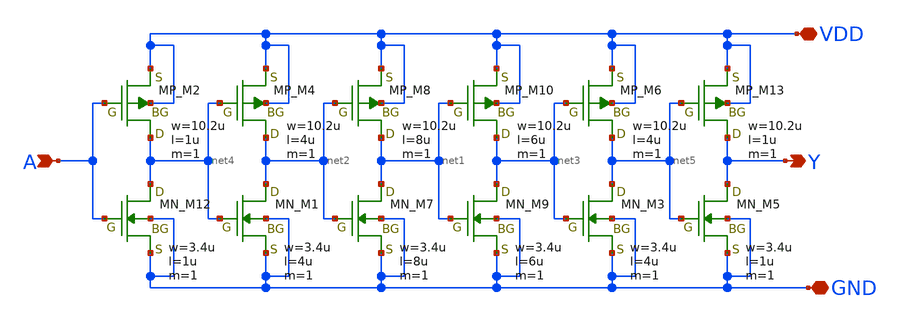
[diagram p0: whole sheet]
** sch_path: libs.tech/xschem/TR-1um_5_stdcell/DEL2.sch
**.subckt DEL2 A Y VDD GND
*.ipin A
*.opin Y
*.iopin VDD
*.iopin GND
XM13 Y net5 VDD VDD PMOS w=10.2u l=1u nrd=0 nrs=0 m=1
XM2 net4 A VDD VDD PMOS w=10.2u l=1u nrd=0 nrs=0 m=1
XM4 net2 net4 VDD VDD PMOS w=10.2u l=4u nrd=0 nrs=0 m=1
XM6 net5 net3 VDD VDD PMOS w=10.2u l=4u nrd=0 nrs=0 m=1
XM8 net1 net2 VDD VDD PMOS w=10.2u l=8u nrd=0 nrs=0 m=1
XM10 net3 net1 VDD VDD PMOS w=10.2u l=6u nrd=0 nrs=0 m=1
XM12 net4 A GND GND NMOS w=3.4u l=1u nrd=0 nrs=0 m=1
XM5 Y net5 GND GND NMOS w=3.4u l=1u nrd=0 nrs=0 m=1
XM1 net2 net4 GND GND NMOS w=3.4u l=4u nrd=0 nrs=0 m=1
XM3 net5 net3 GND GND NMOS w=3.4u l=4u nrd=0 nrs=0 m=1
XM7 net1 net2 GND GND NMOS w=3.4u l=8u nrd=0 nrs=0 m=1
XM9 net3 net1 GND GND NMOS w=3.4u l=6u nrd=0 nrs=0 m=1
**.ends
.end
